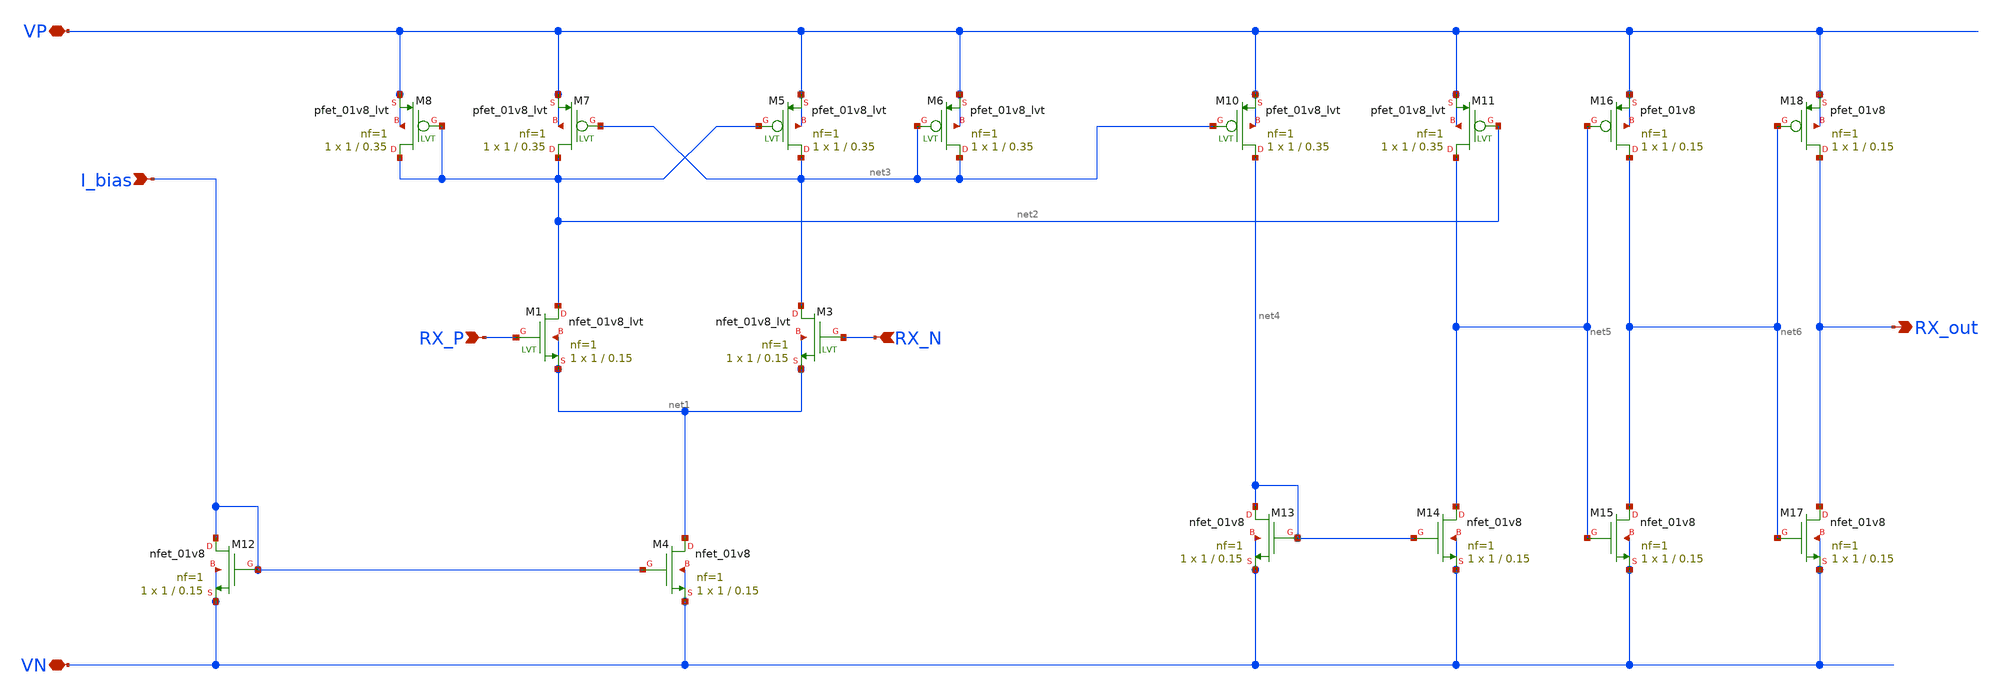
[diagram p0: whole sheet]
** sch_path: xschem/lvds/receiver.sch
**.subckt receiver RX_P VP RX_out RX_N VN I_bias
*.ipin RX_P
*.iopin VP
*.opin RX_out
*.ipin RX_N
*.iopin VN
*.ipin I_bias
XM1 net2 RX_P net1 net1 sky130_fd_pr__nfet_01v8_lvt L=0.15 W=1 nf=1 ad='int((nf+1)/2) * W/nf * 0.29'
+ as='int((nf+2)/2) * W/nf * 0.29' pd='2*int((nf+1)/2) * (W/nf + 0.29)' ps='2*int((nf+2)/2) * (W/nf + 0.29)'
+ nrd='0.29 / W' nrs='0.29 / W' sa=0 sb=0 sd=0 mult=1 m=1
XM3 net3 RX_N net1 net1 sky130_fd_pr__nfet_01v8_lvt L=0.15 W=1 nf=1 ad='int((nf+1)/2) * W/nf * 0.29'
+ as='int((nf+2)/2) * W/nf * 0.29' pd='2*int((nf+1)/2) * (W/nf + 0.29)' ps='2*int((nf+2)/2) * (W/nf + 0.29)'
+ nrd='0.29 / W' nrs='0.29 / W' sa=0 sb=0 sd=0 mult=1 m=1
XM4 net1 I_bias VN VN sky130_fd_pr__nfet_01v8 L=0.15 W=1 nf=1 ad='int((nf+1)/2) * W/nf * 0.29' as='int((nf+2)/2) * W/nf * 0.29'
+ pd='2*int((nf+1)/2) * (W/nf + 0.29)' ps='2*int((nf+2)/2) * (W/nf + 0.29)' nrd='0.29 / W' nrs='0.29 / W'
+ sa=0 sb=0 sd=0 mult=1 m=1
XM7 net2 net3 VP VP sky130_fd_pr__pfet_01v8_lvt L=0.35 W=1 nf=1 ad='int((nf+1)/2) * W/nf * 0.29' as='int((nf+2)/2) * W/nf * 0.29'
+ pd='2*int((nf+1)/2) * (W/nf + 0.29)' ps='2*int((nf+2)/2) * (W/nf + 0.29)' nrd='0.29 / W' nrs='0.29 / W'
+ sa=0 sb=0 sd=0 mult=1 m=1
XM8 net2 net2 VP VP sky130_fd_pr__pfet_01v8_lvt L=0.35 W=1 nf=1 ad='int((nf+1)/2) * W/nf * 0.29' as='int((nf+2)/2) * W/nf * 0.29'
+ pd='2*int((nf+1)/2) * (W/nf + 0.29)' ps='2*int((nf+2)/2) * (W/nf + 0.29)' nrd='0.29 / W' nrs='0.29 / W'
+ sa=0 sb=0 sd=0 mult=1 m=1
XM5 net3 net2 VP VP sky130_fd_pr__pfet_01v8_lvt L=0.35 W=1 nf=1 ad='int((nf+1)/2) * W/nf * 0.29' as='int((nf+2)/2) * W/nf * 0.29'
+ pd='2*int((nf+1)/2) * (W/nf + 0.29)' ps='2*int((nf+2)/2) * (W/nf + 0.29)' nrd='0.29 / W' nrs='0.29 / W'
+ sa=0 sb=0 sd=0 mult=1 m=1
XM6 net3 net3 VP VP sky130_fd_pr__pfet_01v8_lvt L=0.35 W=1 nf=1 ad='int((nf+1)/2) * W/nf * 0.29' as='int((nf+2)/2) * W/nf * 0.29'
+ pd='2*int((nf+1)/2) * (W/nf + 0.29)' ps='2*int((nf+2)/2) * (W/nf + 0.29)' nrd='0.29 / W' nrs='0.29 / W'
+ sa=0 sb=0 sd=0 mult=1 m=1
XM10 net4 net3 VP VP sky130_fd_pr__pfet_01v8_lvt L=0.35 W=1 nf=1 ad='int((nf+1)/2) * W/nf * 0.29' as='int((nf+2)/2) * W/nf * 0.29'
+ pd='2*int((nf+1)/2) * (W/nf + 0.29)' ps='2*int((nf+2)/2) * (W/nf + 0.29)' nrd='0.29 / W' nrs='0.29 / W'
+ sa=0 sb=0 sd=0 mult=1 m=1
XM11 net5 net2 VP VP sky130_fd_pr__pfet_01v8_lvt L=0.35 W=1 nf=1 ad='int((nf+1)/2) * W/nf * 0.29' as='int((nf+2)/2) * W/nf * 0.29'
+ pd='2*int((nf+1)/2) * (W/nf + 0.29)' ps='2*int((nf+2)/2) * (W/nf + 0.29)' nrd='0.29 / W' nrs='0.29 / W'
+ sa=0 sb=0 sd=0 mult=1 m=1
XM12 I_bias I_bias VN VN sky130_fd_pr__nfet_01v8 L=0.15 W=1 nf=1 ad='int((nf+1)/2) * W/nf * 0.29' as='int((nf+2)/2) * W/nf * 0.29'
+ pd='2*int((nf+1)/2) * (W/nf + 0.29)' ps='2*int((nf+2)/2) * (W/nf + 0.29)' nrd='0.29 / W' nrs='0.29 / W'
+ sa=0 sb=0 sd=0 mult=1 m=1
XM13 net4 net4 VN VN sky130_fd_pr__nfet_01v8 L=0.15 W=1 nf=1 ad='int((nf+1)/2) * W/nf * 0.29' as='int((nf+2)/2) * W/nf * 0.29'
+ pd='2*int((nf+1)/2) * (W/nf + 0.29)' ps='2*int((nf+2)/2) * (W/nf + 0.29)' nrd='0.29 / W' nrs='0.29 / W'
+ sa=0 sb=0 sd=0 mult=1 m=1
XM14 net5 net4 VN VN sky130_fd_pr__nfet_01v8 L=0.15 W=1 nf=1 ad='int((nf+1)/2) * W/nf * 0.29' as='int((nf+2)/2) * W/nf * 0.29'
+ pd='2*int((nf+1)/2) * (W/nf + 0.29)' ps='2*int((nf+2)/2) * (W/nf + 0.29)' nrd='0.29 / W' nrs='0.29 / W'
+ sa=0 sb=0 sd=0 mult=1 m=1
XM15 net6 net5 VN VN sky130_fd_pr__nfet_01v8 L=0.15 W=1 nf=1 ad='int((nf+1)/2) * W/nf * 0.29' as='int((nf+2)/2) * W/nf * 0.29'
+ pd='2*int((nf+1)/2) * (W/nf + 0.29)' ps='2*int((nf+2)/2) * (W/nf + 0.29)' nrd='0.29 / W' nrs='0.29 / W'
+ sa=0 sb=0 sd=0 mult=1 m=1
XM16 net6 net5 VP VP sky130_fd_pr__pfet_01v8 L=0.15 W=1 nf=1 ad='int((nf+1)/2) * W/nf * 0.29' as='int((nf+2)/2) * W/nf * 0.29'
+ pd='2*int((nf+1)/2) * (W/nf + 0.29)' ps='2*int((nf+2)/2) * (W/nf + 0.29)' nrd='0.29 / W' nrs='0.29 / W'
+ sa=0 sb=0 sd=0 mult=1 m=1
XM17 RX_out net6 VN VN sky130_fd_pr__nfet_01v8 L=0.15 W=1 nf=1 ad='int((nf+1)/2) * W/nf * 0.29' as='int((nf+2)/2) * W/nf * 0.29'
+ pd='2*int((nf+1)/2) * (W/nf + 0.29)' ps='2*int((nf+2)/2) * (W/nf + 0.29)' nrd='0.29 / W' nrs='0.29 / W'
+ sa=0 sb=0 sd=0 mult=1 m=1
XM18 RX_out net6 VP VP sky130_fd_pr__pfet_01v8 L=0.15 W=1 nf=1 ad='int((nf+1)/2) * W/nf * 0.29' as='int((nf+2)/2) * W/nf * 0.29'
+ pd='2*int((nf+1)/2) * (W/nf + 0.29)' ps='2*int((nf+2)/2) * (W/nf + 0.29)' nrd='0.29 / W' nrs='0.29 / W'
+ sa=0 sb=0 sd=0 mult=1 m=1
**.ends
.end
